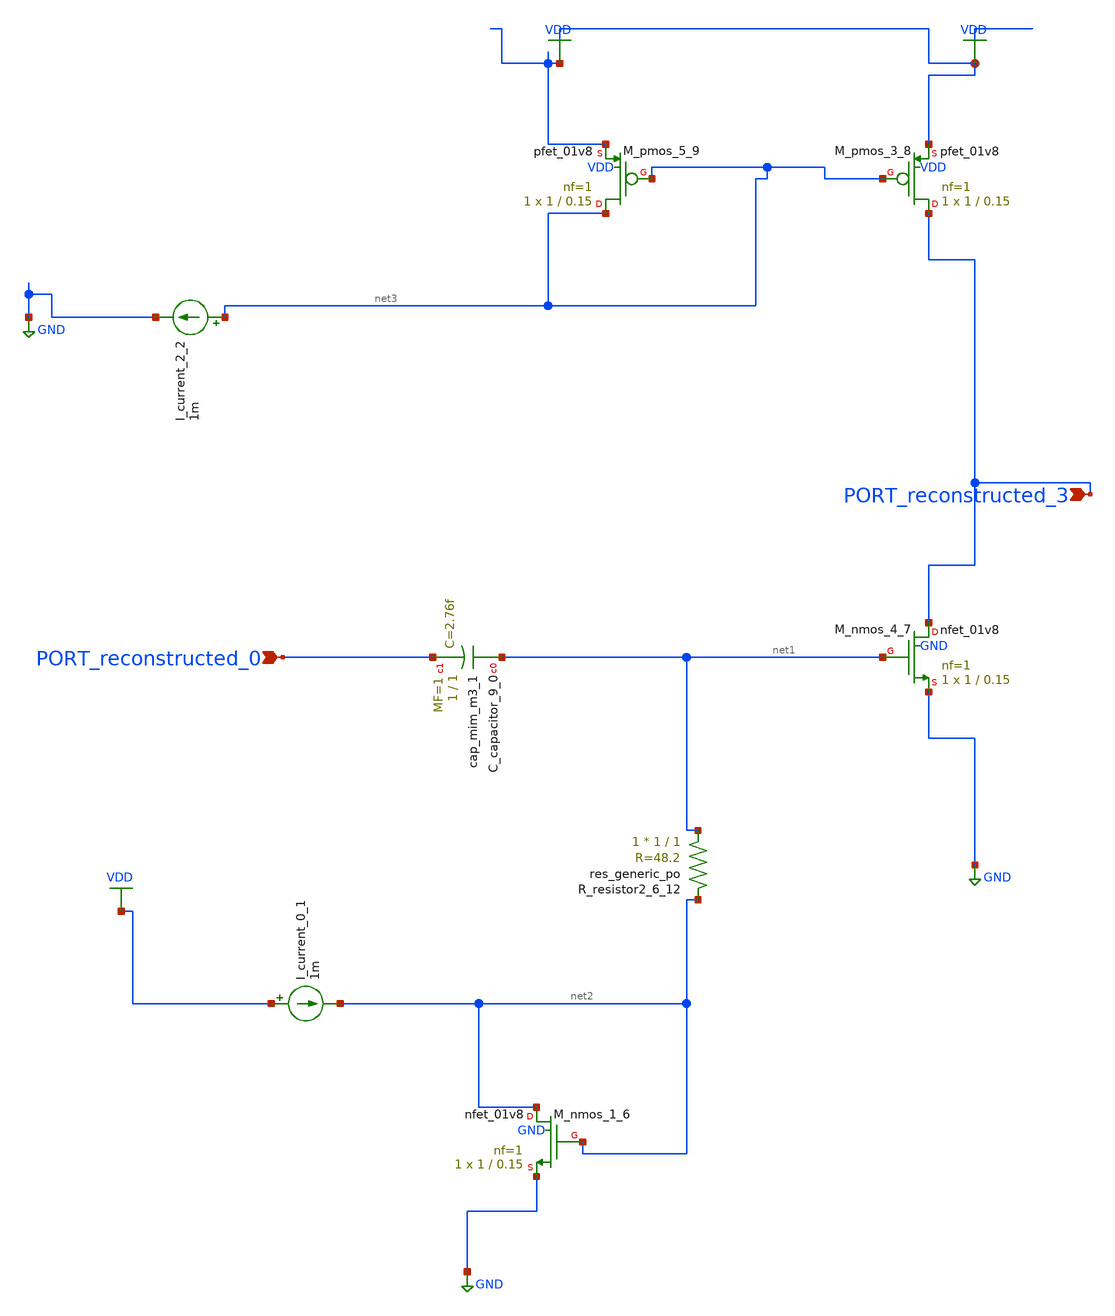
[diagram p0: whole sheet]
** sch_path: schematics/AMSNet/305.sch
**.subckt 305 PORT_reconstructed_3 PORT_reconstructed_0
*.ipin PORT_reconstructed_3
*.ipin PORT_reconstructed_0
XC_capacitor_9_0 net1 PORT_reconstructed_0 sky130_fd_pr__cap_mim_m3_1 W=1 L=1 MF=1 m=1
I_current_0_1 VDD net2 1m
I_current_2_2 net3 GND 1m
XM_nmos_1_6 net2 net2 GND GND sky130_fd_pr__nfet_01v8 L=0.15 W=1 nf=1 ad='int((1 + 1)/2) * 1 / 1 * 0.29'
+ as='int((1 + 2)/2) * 1 / 1 * 0.29' pd='2*int((1 + 1)/2) * (1 / 1 + 0.29)' ps='2*int((1 + 2)/2) * (1 / 1 + 0.29)'
+ nrd='0.29 / 1 ' nrs='0.29 / 1 ' sa=0 sb=0 sd=0 mult=1 m=1
XM_nmos_4_7 PORT_reconstructed_3 net1 GND GND sky130_fd_pr__nfet_01v8 L=0.15 W=1 nf=1 ad='int((1 + 1)/2) * 1 / 1 * 0.29'
+ as='int((1 + 2)/2) * 1 / 1 * 0.29' pd='2*int((1 + 1)/2) * (1 / 1 + 0.29)' ps='2*int((1 + 2)/2) * (1 / 1 + 0.29)'
+ nrd='0.29 / 1 ' nrs='0.29 / 1 ' sa=0 sb=0 sd=0 mult=1 m=1
XM_pmos_3_8 PORT_reconstructed_3 net3 VDD VDD sky130_fd_pr__pfet_01v8 L=0.15 W=1 nf=1 ad='int((1 + 1)/2) * 1 / 1 * 0.29'
+ as='int((1 + 2)/2) * 1 / 1 * 0.29' pd='2*int((1 + 1)/2) * (1 / 1 + 0.29)' ps='2*int((1 + 2)/2) * (1 / 1 + 0.29)'
+ nrd='0.29 / 1 ' nrs='0.29 / 1 ' sa=0 sb=0 sd=0 mult=1 m=1
XM_pmos_5_9 net3 net3 VDD VDD sky130_fd_pr__pfet_01v8 L=0.15 W=1 nf=1 ad='int((1 + 1)/2) * 1 / 1 * 0.29'
+ as='int((1 + 2)/2) * 1 / 1 * 0.29' pd='2*int((1 + 1)/2) * (1 / 1 + 0.29)' ps='2*int((1 + 2)/2) * (1 / 1 + 0.29)'
+ nrd='0.29 / 1 ' nrs='0.29 / 1 ' sa=0 sb=0 sd=0 mult=1 m=1
XR_resistor2_6_12 net1 net2 sky130_fd_pr__res_generic_po W=1 L=1 m=1
**.ends
.GLOBAL GND
.GLOBAL VDD
.end
